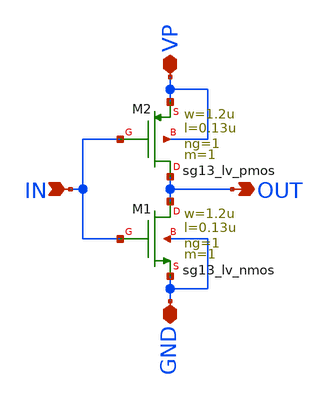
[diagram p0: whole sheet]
** sch_path: schematics/divider/schematics/inverter_x16.sch
**.subckt inverter_x16 IN VP OUT GND
*.ipin IN
*.iopin VP
*.opin OUT
*.iopin GND
XM1 OUT IN GND GND sg13_lv_nmos w=1.2u l=0.13u ng=1 m=1 mm_ok=1
XM2 OUT IN VP VP sg13_lv_pmos w=1.2u l=0.13u ng=1 m=1 mm_ok=1
**.ends
.end
